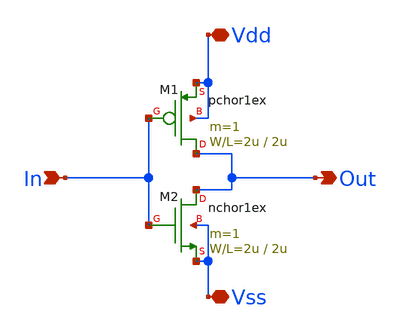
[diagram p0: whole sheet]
** sch_path: member_project/tomoya_nonymous/myinverter.sch
**.subckt myinverter In Vdd Vss Out
*.ipin In
*.iopin Vdd
*.iopin Vss
*.opin Out
M1 Out In Vdd Vdd pchor1ex L=2u W=2u m=1
M2 Out In Vss Vss nchor1ex L=2u W=2u m=1
**.ends
.end
